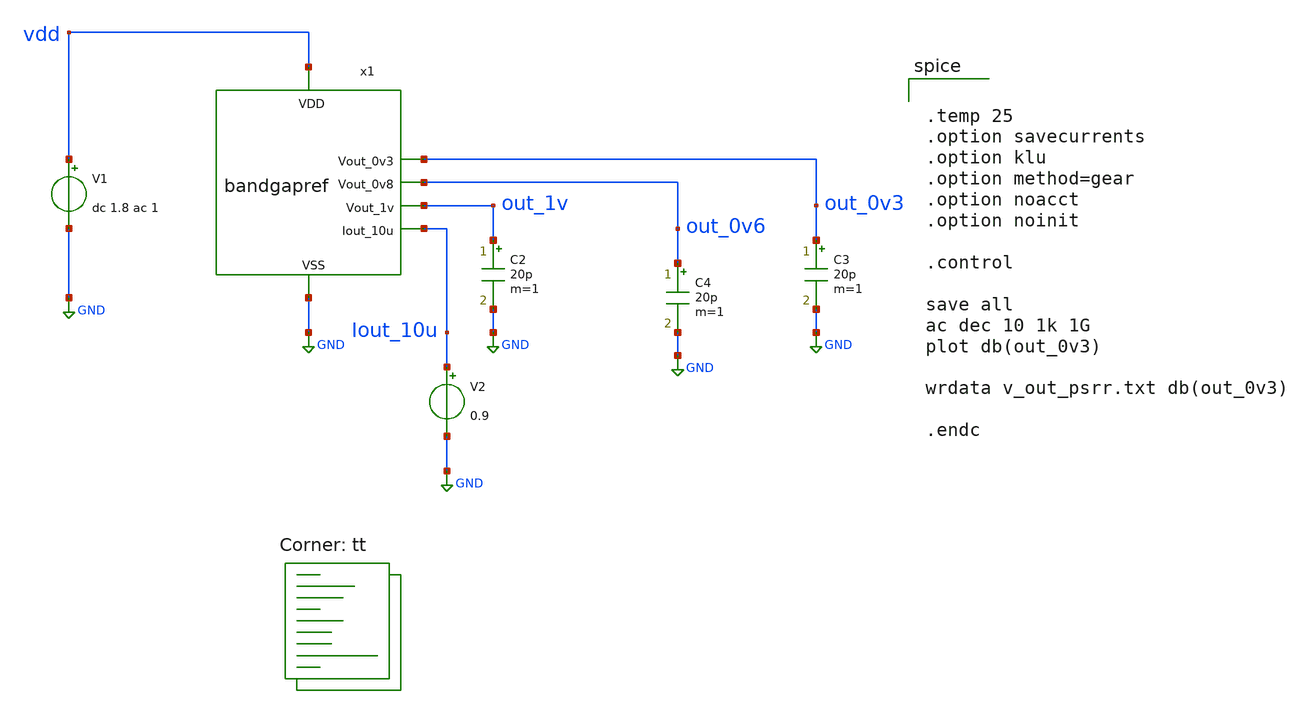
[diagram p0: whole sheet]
** sch_path: xschem/bandgapref_psrr_tb.sch
**.subckt bandgapref_psrr_tb
V1 vdd GND dc 1.8 ac 1
.save i(v1)
x1 vdd out_0v3 GND out_1v out_0v6 Iout_10u bandgapref
C2 out_1v GND 20p m=1
C3 out_0v3 GND 20p m=1
C4 out_0v6 GND 20p m=1
V2 Iout_10u GND 0.9
.save i(v2)
**** begin user architecture code
.lib $::SKYWATER_MODELS/sky130.lib.spice tt


.temp 25
.option savecurrents
.option klu
.option method=gear
.option noacct
.option noinit

.control

save all
ac dec 10 1k 1G
plot db(out_0v3)

wrdata v_out_psrr.txt db(out_0v3)

.endc

**** end user architecture code
**.ends
.GLOBAL GND
.end
